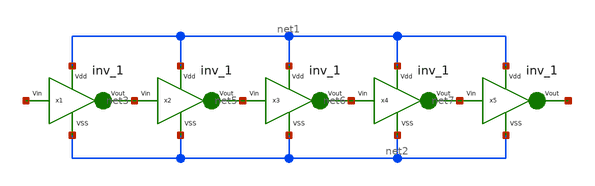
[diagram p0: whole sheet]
** sch_path: xschem files/ring_osc.sch
**.subckt ring_osc
x1 net1 net3 net4 net2 inv_1
x2 net1 net5 net3 net2 inv_1
x3 net1 net6 net5 net2 inv_1
x4 net1 net7 net6 net2 inv_1
x5 net1 net8 net7 net2 inv_1
**.ends

* expanding   symbol:  /home/harshit/.xschem/inv_1.sym # of pins=4
** sym_path: xschem files/inv_1.sym
** sch_path: xschem files/inv_1.sch
.subckt inv_1 Vdd Vout Vin VSS
*.ipin Vdd
*.ipin VSS
*.opin Vout
*.ipin Vin
XM1 Vout Vin VSS VSS sky130_fd_pr__nfet_01v8 L=0.15 W=1.05 nf=1 ad='int((nf+1)/2) * W/nf * 0.29' as='int((nf+2)/2) * W/nf * 0.29'
+ pd='2*int((nf+1)/2) * (W/nf + 0.29)' ps='2*int((nf+2)/2) * (W/nf + 0.29)' nrd='0.29 / W' nrs='0.29 / W'
+ sa=0 sb=0 sd=0 mult=1 m=1
XM2 Vout Vin Vdd Vdd sky130_fd_pr__pfet_01v8 L=0.15 W=2.1 nf=1 ad='int((nf+1)/2) * W/nf * 0.29' as='int((nf+2)/2) * W/nf * 0.29'
+ pd='2*int((nf+1)/2) * (W/nf + 0.29)' ps='2*int((nf+2)/2) * (W/nf + 0.29)' nrd='0.29 / W' nrs='0.29 / W'
+ sa=0 sb=0 sd=0 mult=1 m=1
.ends

.end
